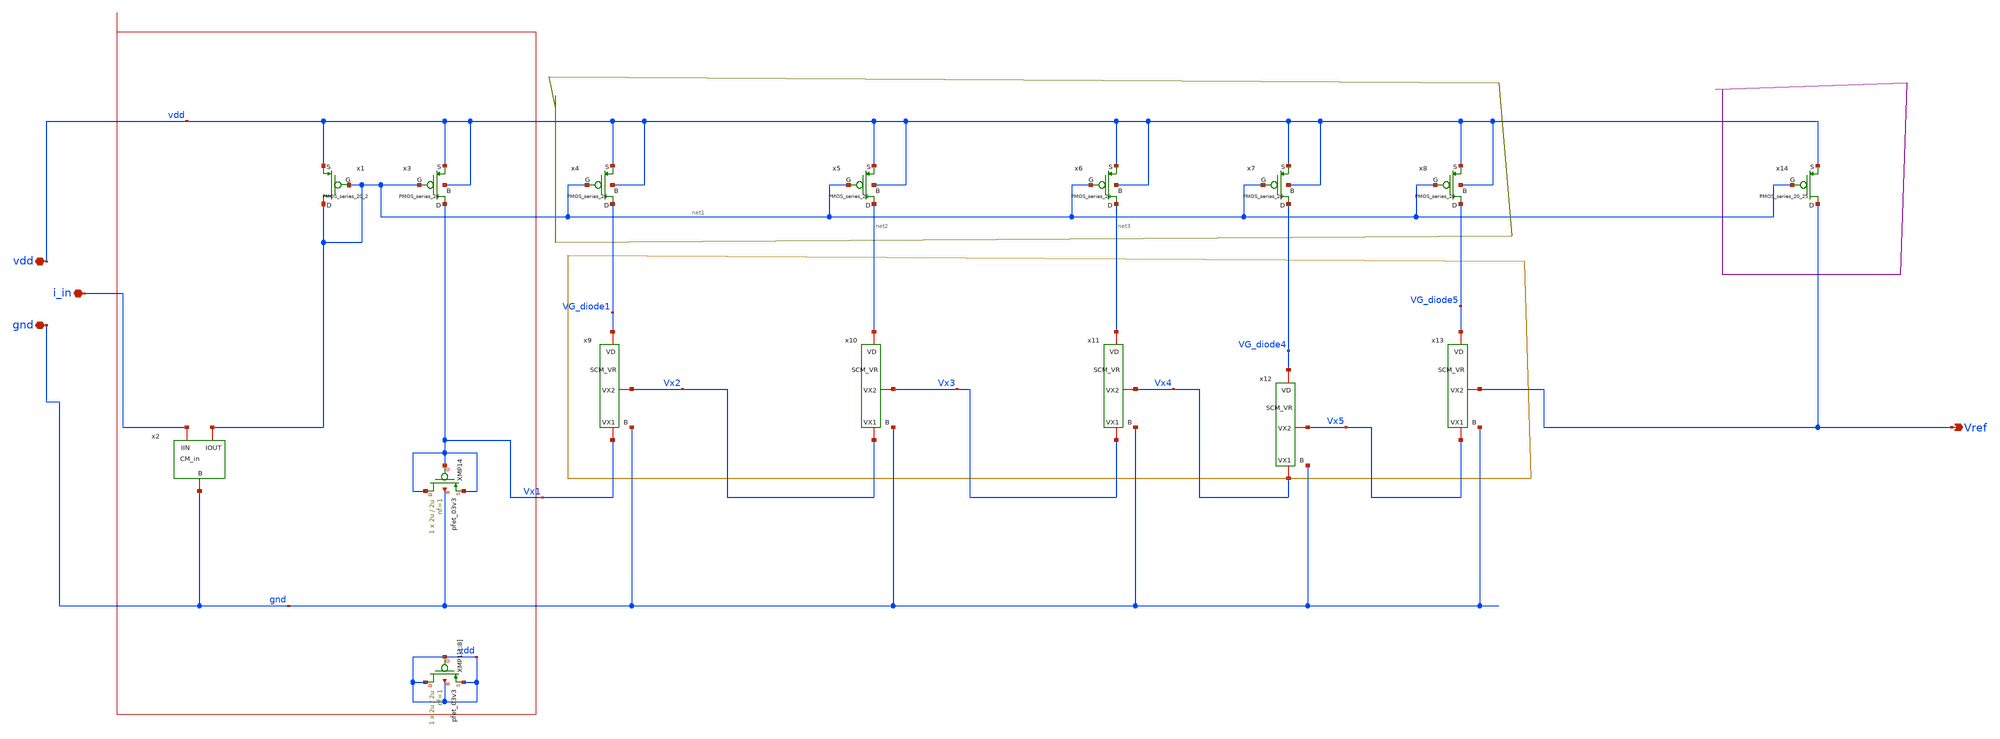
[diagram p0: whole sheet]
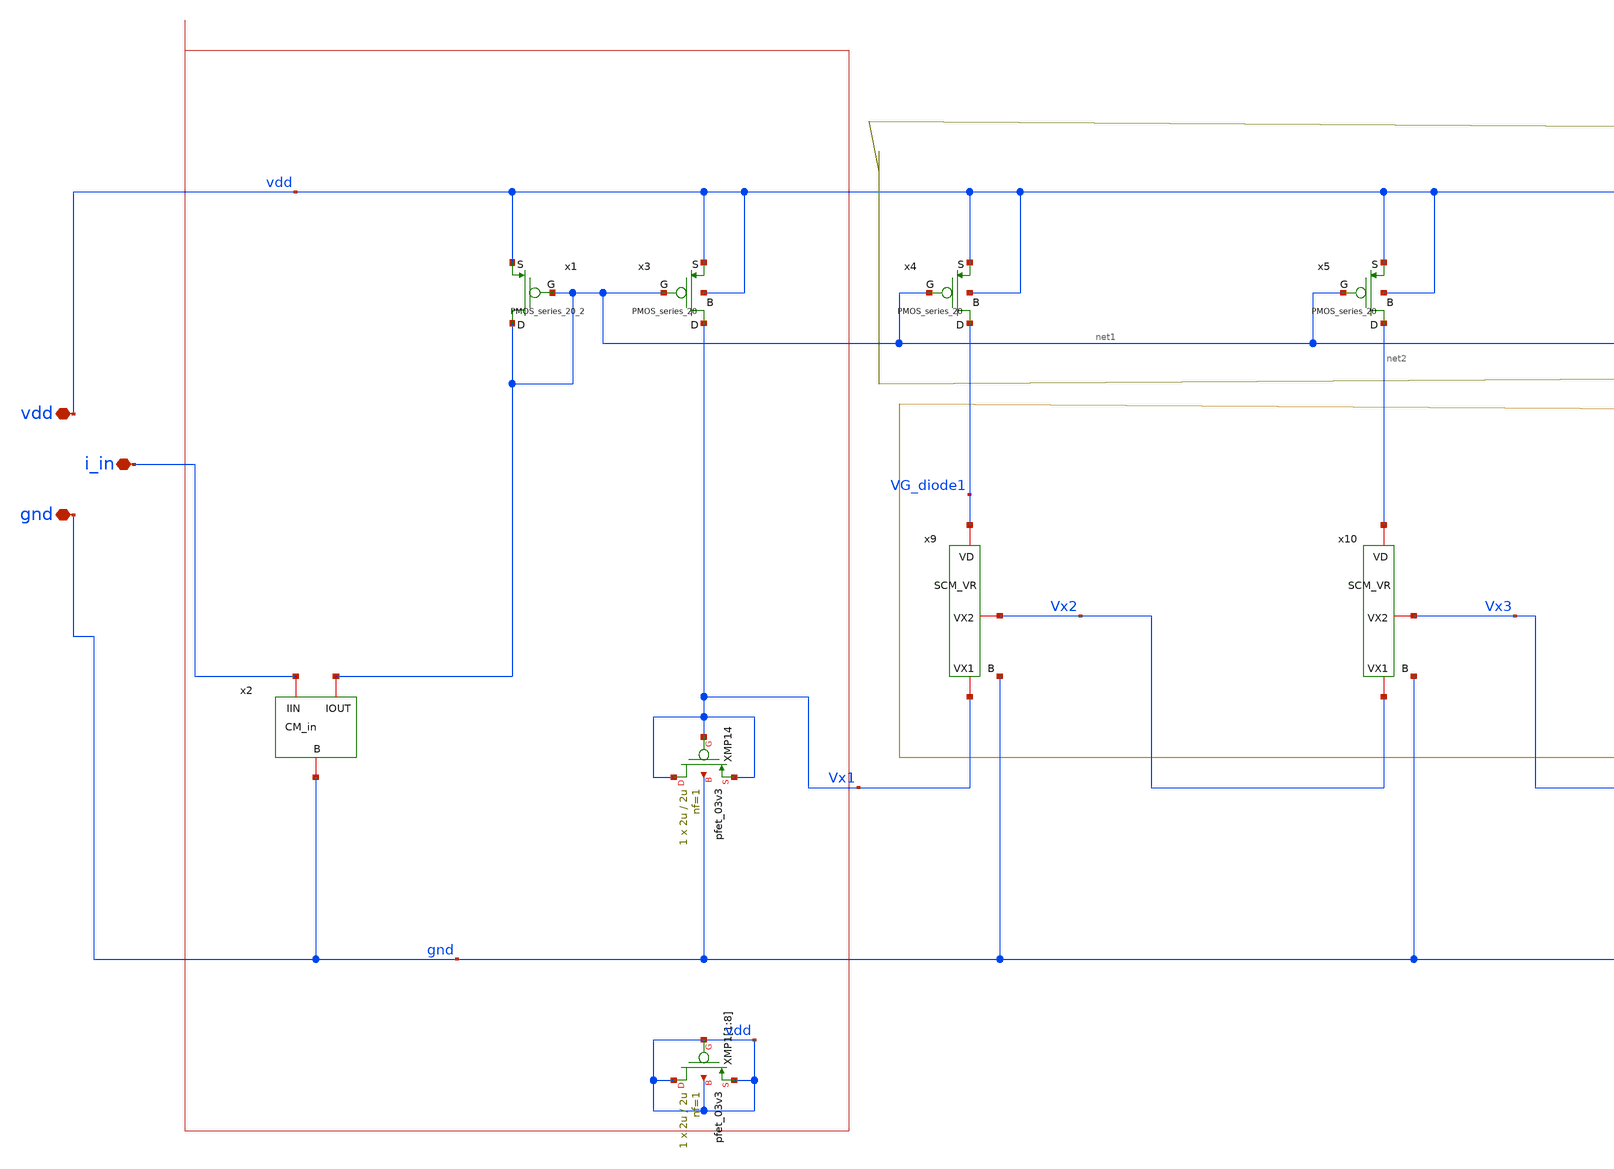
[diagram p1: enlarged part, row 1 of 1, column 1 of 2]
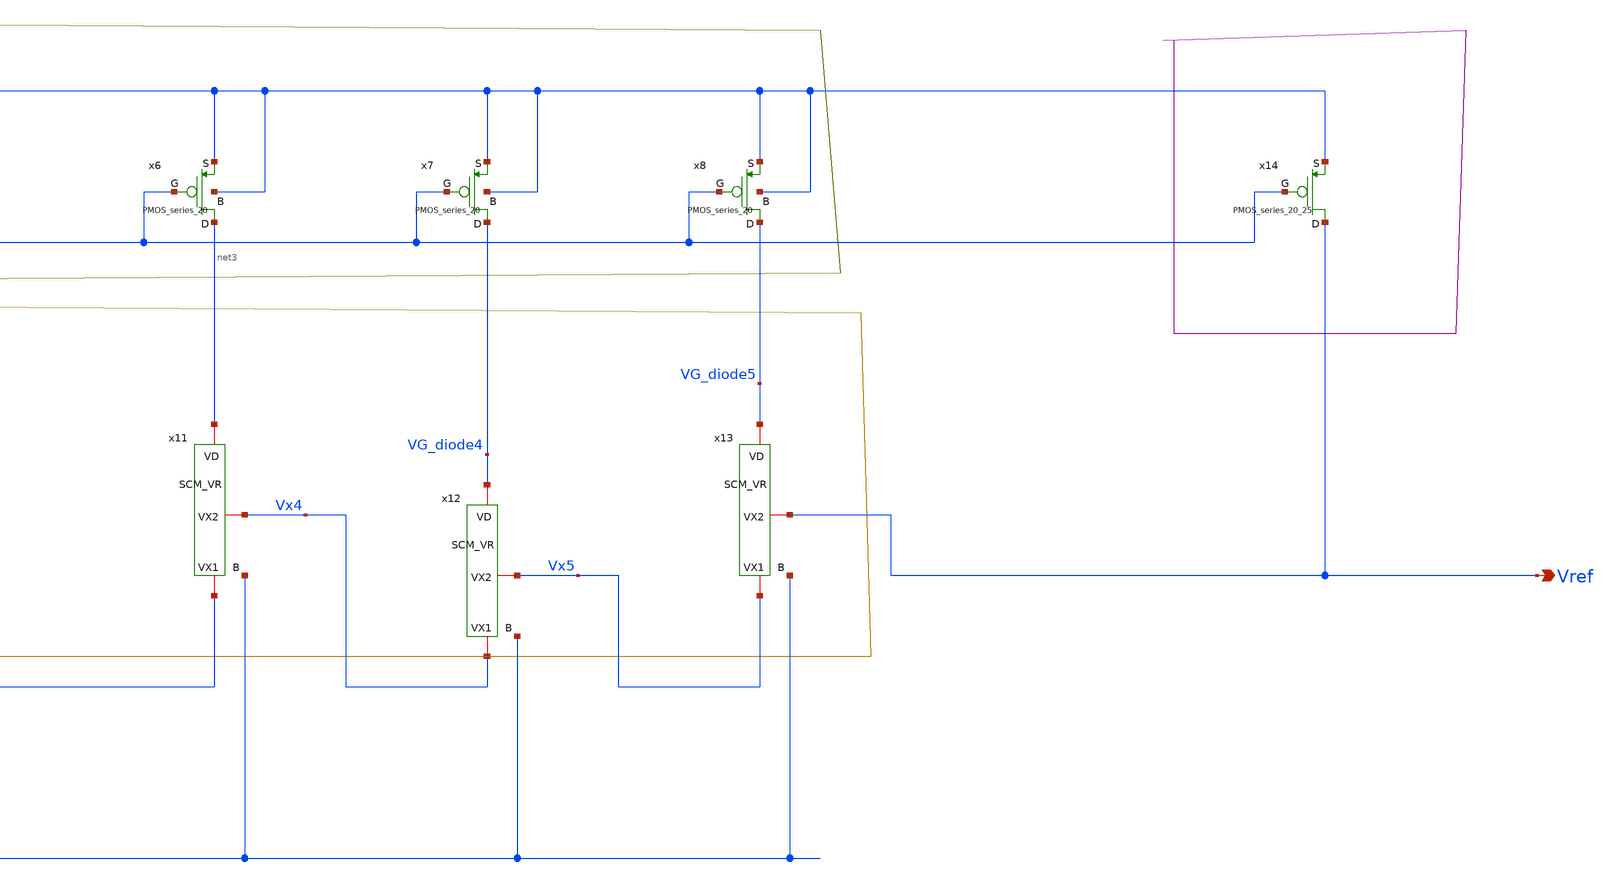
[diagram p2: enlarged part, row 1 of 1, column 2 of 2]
** sch_path: Voltage_Reference/symbols_vr/Voltage_Reference.sch
**.subckt Voltage_Reference i_in vdd gnd Vref
*.iopin i_in
*.iopin vdd
*.iopin gnd
*.opin Vref
XMP14 Vx1 Vx1 Vx1 gnd pfet_03v3 L=2u W=2u nf=1 ad='int((nf+1)/2) * W/nf * 0.18u' as='int((nf+2)/2) * W/nf * 0.18u'
+ pd='2*int((nf+1)/2) * (W/nf + 0.18u)' ps='2*int((nf+2)/2) * (W/nf + 0.18u)' nrd='0.18u / W' nrs='0.18u / W'
+ sa=0 sb=0 sd=0 m=1
x3 vdd Vx1 vdd net1 PMOS_series_20
x4 vdd VG_diode1 vdd net1 PMOS_series_20
x5 vdd net2 vdd net1 PMOS_series_20
x6 vdd net3 vdd net1 PMOS_series_20
x7 vdd VG_diode4 vdd net1 PMOS_series_20
x8 vdd VG_diode5 vdd net1 PMOS_series_20
x9 VG_diode1 Vx1 Vx2 gnd SCM_VR
x10 net2 Vx2 Vx3 gnd SCM_VR
x11 net3 Vx3 Vx4 gnd SCM_VR
x12 VG_diode4 Vx4 Vx5 gnd SCM_VR
x13 VG_diode5 Vx5 Vref gnd SCM_VR
x14 vdd Vref net1 PMOS_series_20_25
x1 vdd net1 net1 PMOS_series_20_2
x2 i_in net1 gnd CM_in
XMP1[1] vdd vdd vdd vdd pfet_03v3 L=2u W=2u nf=1 ad='int((nf+1)/2) * W/nf * 0.18u' as='int((nf+2)/2) * W/nf * 0.18u'
+ pd='2*int((nf+1)/2) * (W/nf + 0.18u)' ps='2*int((nf+2)/2) * (W/nf + 0.18u)' nrd='0.18u / W' nrs='0.18u / W'
+ sa=0 sb=0 sd=0 m=1
XMP1[2] vdd vdd vdd vdd pfet_03v3 L=2u W=2u nf=1 ad='int((nf+1)/2) * W/nf * 0.18u' as='int((nf+2)/2) * W/nf * 0.18u'
+ pd='2*int((nf+1)/2) * (W/nf + 0.18u)' ps='2*int((nf+2)/2) * (W/nf + 0.18u)' nrd='0.18u / W' nrs='0.18u / W'
+ sa=0 sb=0 sd=0 m=1
XMP1[3] vdd vdd vdd vdd pfet_03v3 L=2u W=2u nf=1 ad='int((nf+1)/2) * W/nf * 0.18u' as='int((nf+2)/2) * W/nf * 0.18u'
+ pd='2*int((nf+1)/2) * (W/nf + 0.18u)' ps='2*int((nf+2)/2) * (W/nf + 0.18u)' nrd='0.18u / W' nrs='0.18u / W'
+ sa=0 sb=0 sd=0 m=1
XMP1[4] vdd vdd vdd vdd pfet_03v3 L=2u W=2u nf=1 ad='int((nf+1)/2) * W/nf * 0.18u' as='int((nf+2)/2) * W/nf * 0.18u'
+ pd='2*int((nf+1)/2) * (W/nf + 0.18u)' ps='2*int((nf+2)/2) * (W/nf + 0.18u)' nrd='0.18u / W' nrs='0.18u / W'
+ sa=0 sb=0 sd=0 m=1
XMP1[5] vdd vdd vdd vdd pfet_03v3 L=2u W=2u nf=1 ad='int((nf+1)/2) * W/nf * 0.18u' as='int((nf+2)/2) * W/nf * 0.18u'
+ pd='2*int((nf+1)/2) * (W/nf + 0.18u)' ps='2*int((nf+2)/2) * (W/nf + 0.18u)' nrd='0.18u / W' nrs='0.18u / W'
+ sa=0 sb=0 sd=0 m=1
XMP1[6] vdd vdd vdd vdd pfet_03v3 L=2u W=2u nf=1 ad='int((nf+1)/2) * W/nf * 0.18u' as='int((nf+2)/2) * W/nf * 0.18u'
+ pd='2*int((nf+1)/2) * (W/nf + 0.18u)' ps='2*int((nf+2)/2) * (W/nf + 0.18u)' nrd='0.18u / W' nrs='0.18u / W'
+ sa=0 sb=0 sd=0 m=1
XMP1[7] vdd vdd vdd vdd pfet_03v3 L=2u W=2u nf=1 ad='int((nf+1)/2) * W/nf * 0.18u' as='int((nf+2)/2) * W/nf * 0.18u'
+ pd='2*int((nf+1)/2) * (W/nf + 0.18u)' ps='2*int((nf+2)/2) * (W/nf + 0.18u)' nrd='0.18u / W' nrs='0.18u / W'
+ sa=0 sb=0 sd=0 m=1
XMP1[8] vdd vdd vdd vdd pfet_03v3 L=2u W=2u nf=1 ad='int((nf+1)/2) * W/nf * 0.18u' as='int((nf+2)/2) * W/nf * 0.18u'
+ pd='2*int((nf+1)/2) * (W/nf + 0.18u)' ps='2*int((nf+2)/2) * (W/nf + 0.18u)' nrd='0.18u / W' nrs='0.18u / W'
+ sa=0 sb=0 sd=0 m=1
**.ends

* expanding   symbol:  symbols_vr/PMOS_series_20.sym # of pins=4
** sym_path: Voltage_Reference/symbols_vr/PMOS_series_20.sym
** sch_path: Voltage_Reference/symbols_vr/PMOS_series_20.sch
.subckt PMOS_series_20 S D B G
*.iopin S
*.iopin D
*.iopin B
*.iopin G
XMP1 net1 G S B pfet_03v3 L=2u W=2u nf=1 ad='int((nf+1)/2) * W/nf * 0.18u' as='int((nf+2)/2) * W/nf * 0.18u'
+ pd='2*int((nf+1)/2) * (W/nf + 0.18u)' ps='2*int((nf+2)/2) * (W/nf + 0.18u)' nrd='0.18u / W' nrs='0.18u / W'
+ sa=0 sb=0 sd=0 m=1
XMP2 net3 G net1 B pfet_03v3 L=2u W=2u nf=1 ad='int((nf+1)/2) * W/nf * 0.18u' as='int((nf+2)/2) * W/nf * 0.18u'
+ pd='2*int((nf+1)/2) * (W/nf + 0.18u)' ps='2*int((nf+2)/2) * (W/nf + 0.18u)' nrd='0.18u / W' nrs='0.18u / W'
+ sa=0 sb=0 sd=0 m=1
XMP3 net2 G net3 B pfet_03v3 L=2u W=2u nf=1 ad='int((nf+1)/2) * W/nf * 0.18u' as='int((nf+2)/2) * W/nf * 0.18u'
+ pd='2*int((nf+1)/2) * (W/nf + 0.18u)' ps='2*int((nf+2)/2) * (W/nf + 0.18u)' nrd='0.18u / W' nrs='0.18u / W'
+ sa=0 sb=0 sd=0 m=1
XMP4 net5 G net2 B pfet_03v3 L=2u W=2u nf=1 ad='int((nf+1)/2) * W/nf * 0.18u' as='int((nf+2)/2) * W/nf * 0.18u'
+ pd='2*int((nf+1)/2) * (W/nf + 0.18u)' ps='2*int((nf+2)/2) * (W/nf + 0.18u)' nrd='0.18u / W' nrs='0.18u / W'
+ sa=0 sb=0 sd=0 m=1
XMP5 net4 G net5 B pfet_03v3 L=2u W=2u nf=1 ad='int((nf+1)/2) * W/nf * 0.18u' as='int((nf+2)/2) * W/nf * 0.18u'
+ pd='2*int((nf+1)/2) * (W/nf + 0.18u)' ps='2*int((nf+2)/2) * (W/nf + 0.18u)' nrd='0.18u / W' nrs='0.18u / W'
+ sa=0 sb=0 sd=0 m=1
XMP6 net7 G net4 B pfet_03v3 L=2u W=2u nf=1 ad='int((nf+1)/2) * W/nf * 0.18u' as='int((nf+2)/2) * W/nf * 0.18u'
+ pd='2*int((nf+1)/2) * (W/nf + 0.18u)' ps='2*int((nf+2)/2) * (W/nf + 0.18u)' nrd='0.18u / W' nrs='0.18u / W'
+ sa=0 sb=0 sd=0 m=1
XMP7 net6 G net7 B pfet_03v3 L=2u W=2u nf=1 ad='int((nf+1)/2) * W/nf * 0.18u' as='int((nf+2)/2) * W/nf * 0.18u'
+ pd='2*int((nf+1)/2) * (W/nf + 0.18u)' ps='2*int((nf+2)/2) * (W/nf + 0.18u)' nrd='0.18u / W' nrs='0.18u / W'
+ sa=0 sb=0 sd=0 m=1
XMP8 net9 G net6 B pfet_03v3 L=2u W=2u nf=1 ad='int((nf+1)/2) * W/nf * 0.18u' as='int((nf+2)/2) * W/nf * 0.18u'
+ pd='2*int((nf+1)/2) * (W/nf + 0.18u)' ps='2*int((nf+2)/2) * (W/nf + 0.18u)' nrd='0.18u / W' nrs='0.18u / W'
+ sa=0 sb=0 sd=0 m=1
XMP9 net8 G net9 B pfet_03v3 L=2u W=2u nf=1 ad='int((nf+1)/2) * W/nf * 0.18u' as='int((nf+2)/2) * W/nf * 0.18u'
+ pd='2*int((nf+1)/2) * (W/nf + 0.18u)' ps='2*int((nf+2)/2) * (W/nf + 0.18u)' nrd='0.18u / W' nrs='0.18u / W'
+ sa=0 sb=0 sd=0 m=1
XMP10 net19 G net8 B pfet_03v3 L=2u W=2u nf=1 ad='int((nf+1)/2) * W/nf * 0.18u' as='int((nf+2)/2) * W/nf * 0.18u'
+ pd='2*int((nf+1)/2) * (W/nf + 0.18u)' ps='2*int((nf+2)/2) * (W/nf + 0.18u)' nrd='0.18u / W' nrs='0.18u / W'
+ sa=0 sb=0 sd=0 m=1
XMP11 net10 G net19 B pfet_03v3 L=2u W=2u nf=1 ad='int((nf+1)/2) * W/nf * 0.18u' as='int((nf+2)/2) * W/nf * 0.18u'
+ pd='2*int((nf+1)/2) * (W/nf + 0.18u)' ps='2*int((nf+2)/2) * (W/nf + 0.18u)' nrd='0.18u / W' nrs='0.18u / W'
+ sa=0 sb=0 sd=0 m=1
XMP12 net12 G net10 B pfet_03v3 L=2u W=2u nf=1 ad='int((nf+1)/2) * W/nf * 0.18u' as='int((nf+2)/2) * W/nf * 0.18u'
+ pd='2*int((nf+1)/2) * (W/nf + 0.18u)' ps='2*int((nf+2)/2) * (W/nf + 0.18u)' nrd='0.18u / W' nrs='0.18u / W'
+ sa=0 sb=0 sd=0 m=1
XMP13 net11 G net12 B pfet_03v3 L=2u W=2u nf=1 ad='int((nf+1)/2) * W/nf * 0.18u' as='int((nf+2)/2) * W/nf * 0.18u'
+ pd='2*int((nf+1)/2) * (W/nf + 0.18u)' ps='2*int((nf+2)/2) * (W/nf + 0.18u)' nrd='0.18u / W' nrs='0.18u / W'
+ sa=0 sb=0 sd=0 m=1
XMP14 net14 G net11 B pfet_03v3 L=2u W=2u nf=1 ad='int((nf+1)/2) * W/nf * 0.18u' as='int((nf+2)/2) * W/nf * 0.18u'
+ pd='2*int((nf+1)/2) * (W/nf + 0.18u)' ps='2*int((nf+2)/2) * (W/nf + 0.18u)' nrd='0.18u / W' nrs='0.18u / W'
+ sa=0 sb=0 sd=0 m=1
XMP15 net13 G net14 B pfet_03v3 L=2u W=2u nf=1 ad='int((nf+1)/2) * W/nf * 0.18u' as='int((nf+2)/2) * W/nf * 0.18u'
+ pd='2*int((nf+1)/2) * (W/nf + 0.18u)' ps='2*int((nf+2)/2) * (W/nf + 0.18u)' nrd='0.18u / W' nrs='0.18u / W'
+ sa=0 sb=0 sd=0 m=1
XMP16 net16 G net13 B pfet_03v3 L=2u W=2u nf=1 ad='int((nf+1)/2) * W/nf * 0.18u' as='int((nf+2)/2) * W/nf * 0.18u'
+ pd='2*int((nf+1)/2) * (W/nf + 0.18u)' ps='2*int((nf+2)/2) * (W/nf + 0.18u)' nrd='0.18u / W' nrs='0.18u / W'
+ sa=0 sb=0 sd=0 m=1
XMP17 net15 G net16 B pfet_03v3 L=2u W=2u nf=1 ad='int((nf+1)/2) * W/nf * 0.18u' as='int((nf+2)/2) * W/nf * 0.18u'
+ pd='2*int((nf+1)/2) * (W/nf + 0.18u)' ps='2*int((nf+2)/2) * (W/nf + 0.18u)' nrd='0.18u / W' nrs='0.18u / W'
+ sa=0 sb=0 sd=0 m=1
XMP18 net18 G net15 B pfet_03v3 L=2u W=2u nf=1 ad='int((nf+1)/2) * W/nf * 0.18u' as='int((nf+2)/2) * W/nf * 0.18u'
+ pd='2*int((nf+1)/2) * (W/nf + 0.18u)' ps='2*int((nf+2)/2) * (W/nf + 0.18u)' nrd='0.18u / W' nrs='0.18u / W'
+ sa=0 sb=0 sd=0 m=1
XMP19 net17 G net18 B pfet_03v3 L=2u W=2u nf=1 ad='int((nf+1)/2) * W/nf * 0.18u' as='int((nf+2)/2) * W/nf * 0.18u'
+ pd='2*int((nf+1)/2) * (W/nf + 0.18u)' ps='2*int((nf+2)/2) * (W/nf + 0.18u)' nrd='0.18u / W' nrs='0.18u / W'
+ sa=0 sb=0 sd=0 m=1
XMP20 D G net17 B pfet_03v3 L=2u W=2u nf=1 ad='int((nf+1)/2) * W/nf * 0.18u' as='int((nf+2)/2) * W/nf * 0.18u'
+ pd='2*int((nf+1)/2) * (W/nf + 0.18u)' ps='2*int((nf+2)/2) * (W/nf + 0.18u)' nrd='0.18u / W' nrs='0.18u / W'
+ sa=0 sb=0 sd=0 m=1
XMP21[1] B B B B pfet_03v3 L=2u W=2u nf=1 ad='int((nf+1)/2) * W/nf * 0.18u' as='int((nf+2)/2) * W/nf * 0.18u'
+ pd='2*int((nf+1)/2) * (W/nf + 0.18u)' ps='2*int((nf+2)/2) * (W/nf + 0.18u)' nrd='0.18u / W' nrs='0.18u / W'
+ sa=0 sb=0 sd=0 m=1
XMP21[2] B B B B pfet_03v3 L=2u W=2u nf=1 ad='int((nf+1)/2) * W/nf * 0.18u' as='int((nf+2)/2) * W/nf * 0.18u'
+ pd='2*int((nf+1)/2) * (W/nf + 0.18u)' ps='2*int((nf+2)/2) * (W/nf + 0.18u)' nrd='0.18u / W' nrs='0.18u / W'
+ sa=0 sb=0 sd=0 m=1
XMP21[3] B B B B pfet_03v3 L=2u W=2u nf=1 ad='int((nf+1)/2) * W/nf * 0.18u' as='int((nf+2)/2) * W/nf * 0.18u'
+ pd='2*int((nf+1)/2) * (W/nf + 0.18u)' ps='2*int((nf+2)/2) * (W/nf + 0.18u)' nrd='0.18u / W' nrs='0.18u / W'
+ sa=0 sb=0 sd=0 m=1
XMP21[4] B B B B pfet_03v3 L=2u W=2u nf=1 ad='int((nf+1)/2) * W/nf * 0.18u' as='int((nf+2)/2) * W/nf * 0.18u'
+ pd='2*int((nf+1)/2) * (W/nf + 0.18u)' ps='2*int((nf+2)/2) * (W/nf + 0.18u)' nrd='0.18u / W' nrs='0.18u / W'
+ sa=0 sb=0 sd=0 m=1
XMP21[5] B B B B pfet_03v3 L=2u W=2u nf=1 ad='int((nf+1)/2) * W/nf * 0.18u' as='int((nf+2)/2) * W/nf * 0.18u'
+ pd='2*int((nf+1)/2) * (W/nf + 0.18u)' ps='2*int((nf+2)/2) * (W/nf + 0.18u)' nrd='0.18u / W' nrs='0.18u / W'
+ sa=0 sb=0 sd=0 m=1
XMP21[6] B B B B pfet_03v3 L=2u W=2u nf=1 ad='int((nf+1)/2) * W/nf * 0.18u' as='int((nf+2)/2) * W/nf * 0.18u'
+ pd='2*int((nf+1)/2) * (W/nf + 0.18u)' ps='2*int((nf+2)/2) * (W/nf + 0.18u)' nrd='0.18u / W' nrs='0.18u / W'
+ sa=0 sb=0 sd=0 m=1
XMP21[7] B B B B pfet_03v3 L=2u W=2u nf=1 ad='int((nf+1)/2) * W/nf * 0.18u' as='int((nf+2)/2) * W/nf * 0.18u'
+ pd='2*int((nf+1)/2) * (W/nf + 0.18u)' ps='2*int((nf+2)/2) * (W/nf + 0.18u)' nrd='0.18u / W' nrs='0.18u / W'
+ sa=0 sb=0 sd=0 m=1
XMP21[8] B B B B pfet_03v3 L=2u W=2u nf=1 ad='int((nf+1)/2) * W/nf * 0.18u' as='int((nf+2)/2) * W/nf * 0.18u'
+ pd='2*int((nf+1)/2) * (W/nf + 0.18u)' ps='2*int((nf+2)/2) * (W/nf + 0.18u)' nrd='0.18u / W' nrs='0.18u / W'
+ sa=0 sb=0 sd=0 m=1
XMP21[9] B B B B pfet_03v3 L=2u W=2u nf=1 ad='int((nf+1)/2) * W/nf * 0.18u' as='int((nf+2)/2) * W/nf * 0.18u'
+ pd='2*int((nf+1)/2) * (W/nf + 0.18u)' ps='2*int((nf+2)/2) * (W/nf + 0.18u)' nrd='0.18u / W' nrs='0.18u / W'
+ sa=0 sb=0 sd=0 m=1
XMP21[10] B B B B pfet_03v3 L=2u W=2u nf=1 ad='int((nf+1)/2) * W/nf * 0.18u' as='int((nf+2)/2) * W/nf * 0.18u'
+ pd='2*int((nf+1)/2) * (W/nf + 0.18u)' ps='2*int((nf+2)/2) * (W/nf + 0.18u)' nrd='0.18u / W' nrs='0.18u / W'
+ sa=0 sb=0 sd=0 m=1
XMP21[11] B B B B pfet_03v3 L=2u W=2u nf=1 ad='int((nf+1)/2) * W/nf * 0.18u' as='int((nf+2)/2) * W/nf * 0.18u'
+ pd='2*int((nf+1)/2) * (W/nf + 0.18u)' ps='2*int((nf+2)/2) * (W/nf + 0.18u)' nrd='0.18u / W' nrs='0.18u / W'
+ sa=0 sb=0 sd=0 m=1
XMP21[12] B B B B pfet_03v3 L=2u W=2u nf=1 ad='int((nf+1)/2) * W/nf * 0.18u' as='int((nf+2)/2) * W/nf * 0.18u'
+ pd='2*int((nf+1)/2) * (W/nf + 0.18u)' ps='2*int((nf+2)/2) * (W/nf + 0.18u)' nrd='0.18u / W' nrs='0.18u / W'
+ sa=0 sb=0 sd=0 m=1
XMP21[13] B B B B pfet_03v3 L=2u W=2u nf=1 ad='int((nf+1)/2) * W/nf * 0.18u' as='int((nf+2)/2) * W/nf * 0.18u'
+ pd='2*int((nf+1)/2) * (W/nf + 0.18u)' ps='2*int((nf+2)/2) * (W/nf + 0.18u)' nrd='0.18u / W' nrs='0.18u / W'
+ sa=0 sb=0 sd=0 m=1
XMP21[14] B B B B pfet_03v3 L=2u W=2u nf=1 ad='int((nf+1)/2) * W/nf * 0.18u' as='int((nf+2)/2) * W/nf * 0.18u'
+ pd='2*int((nf+1)/2) * (W/nf + 0.18u)' ps='2*int((nf+2)/2) * (W/nf + 0.18u)' nrd='0.18u / W' nrs='0.18u / W'
+ sa=0 sb=0 sd=0 m=1
XMP21[15] B B B B pfet_03v3 L=2u W=2u nf=1 ad='int((nf+1)/2) * W/nf * 0.18u' as='int((nf+2)/2) * W/nf * 0.18u'
+ pd='2*int((nf+1)/2) * (W/nf + 0.18u)' ps='2*int((nf+2)/2) * (W/nf + 0.18u)' nrd='0.18u / W' nrs='0.18u / W'
+ sa=0 sb=0 sd=0 m=1
XMP21[16] B B B B pfet_03v3 L=2u W=2u nf=1 ad='int((nf+1)/2) * W/nf * 0.18u' as='int((nf+2)/2) * W/nf * 0.18u'
+ pd='2*int((nf+1)/2) * (W/nf + 0.18u)' ps='2*int((nf+2)/2) * (W/nf + 0.18u)' nrd='0.18u / W' nrs='0.18u / W'
+ sa=0 sb=0 sd=0 m=1
XMP21[17] B B B B pfet_03v3 L=2u W=2u nf=1 ad='int((nf+1)/2) * W/nf * 0.18u' as='int((nf+2)/2) * W/nf * 0.18u'
+ pd='2*int((nf+1)/2) * (W/nf + 0.18u)' ps='2*int((nf+2)/2) * (W/nf + 0.18u)' nrd='0.18u / W' nrs='0.18u / W'
+ sa=0 sb=0 sd=0 m=1
XMP21[18] B B B B pfet_03v3 L=2u W=2u nf=1 ad='int((nf+1)/2) * W/nf * 0.18u' as='int((nf+2)/2) * W/nf * 0.18u'
+ pd='2*int((nf+1)/2) * (W/nf + 0.18u)' ps='2*int((nf+2)/2) * (W/nf + 0.18u)' nrd='0.18u / W' nrs='0.18u / W'
+ sa=0 sb=0 sd=0 m=1
XMP21[19] B B B B pfet_03v3 L=2u W=2u nf=1 ad='int((nf+1)/2) * W/nf * 0.18u' as='int((nf+2)/2) * W/nf * 0.18u'
+ pd='2*int((nf+1)/2) * (W/nf + 0.18u)' ps='2*int((nf+2)/2) * (W/nf + 0.18u)' nrd='0.18u / W' nrs='0.18u / W'
+ sa=0 sb=0 sd=0 m=1
XMP21[20] B B B B pfet_03v3 L=2u W=2u nf=1 ad='int((nf+1)/2) * W/nf * 0.18u' as='int((nf+2)/2) * W/nf * 0.18u'
+ pd='2*int((nf+1)/2) * (W/nf + 0.18u)' ps='2*int((nf+2)/2) * (W/nf + 0.18u)' nrd='0.18u / W' nrs='0.18u / W'
+ sa=0 sb=0 sd=0 m=1
XMP21[21] B B B B pfet_03v3 L=2u W=2u nf=1 ad='int((nf+1)/2) * W/nf * 0.18u' as='int((nf+2)/2) * W/nf * 0.18u'
+ pd='2*int((nf+1)/2) * (W/nf + 0.18u)' ps='2*int((nf+2)/2) * (W/nf + 0.18u)' nrd='0.18u / W' nrs='0.18u / W'
+ sa=0 sb=0 sd=0 m=1
XMP21[22] B B B B pfet_03v3 L=2u W=2u nf=1 ad='int((nf+1)/2) * W/nf * 0.18u' as='int((nf+2)/2) * W/nf * 0.18u'
+ pd='2*int((nf+1)/2) * (W/nf + 0.18u)' ps='2*int((nf+2)/2) * (W/nf + 0.18u)' nrd='0.18u / W' nrs='0.18u / W'
+ sa=0 sb=0 sd=0 m=1
.ends


* expanding   symbol:  symbols_vr/SCM_VR.sym # of pins=4
** sym_path: Voltage_Reference/symbols_vr/SCM_VR.sym
** sch_path: Voltage_Reference/symbols_vr/SCM_VR.sch
.subckt SCM_VR VD VX1 VX2 B
*.iopin VD
*.iopin VX1
*.iopin VX2
*.iopin B
XMN1[1] VD VD VX2 B nfet_03v3 L=2u W=2u nf=1 ad='int((nf+1)/2) * W/nf * 0.18u' as='int((nf+2)/2) * W/nf * 0.18u'
+ pd='2*int((nf+1)/2) * (W/nf + 0.18u)' ps='2*int((nf+2)/2) * (W/nf + 0.18u)' nrd='0.18u / W' nrs='0.18u / W'
+ sa=0 sb=0 sd=0 m=1
XMN1[2] VD VD VX2 B nfet_03v3 L=2u W=2u nf=1 ad='int((nf+1)/2) * W/nf * 0.18u' as='int((nf+2)/2) * W/nf * 0.18u'
+ pd='2*int((nf+1)/2) * (W/nf + 0.18u)' ps='2*int((nf+2)/2) * (W/nf + 0.18u)' nrd='0.18u / W' nrs='0.18u / W'
+ sa=0 sb=0 sd=0 m=1
XMN1[3] VD VD VX2 B nfet_03v3 L=2u W=2u nf=1 ad='int((nf+1)/2) * W/nf * 0.18u' as='int((nf+2)/2) * W/nf * 0.18u'
+ pd='2*int((nf+1)/2) * (W/nf + 0.18u)' ps='2*int((nf+2)/2) * (W/nf + 0.18u)' nrd='0.18u / W' nrs='0.18u / W'
+ sa=0 sb=0 sd=0 m=1
XMN1[4] VD VD VX2 B nfet_03v3 L=2u W=2u nf=1 ad='int((nf+1)/2) * W/nf * 0.18u' as='int((nf+2)/2) * W/nf * 0.18u'
+ pd='2*int((nf+1)/2) * (W/nf + 0.18u)' ps='2*int((nf+2)/2) * (W/nf + 0.18u)' nrd='0.18u / W' nrs='0.18u / W'
+ sa=0 sb=0 sd=0 m=1
XMN1[5] VD VD VX2 B nfet_03v3 L=2u W=2u nf=1 ad='int((nf+1)/2) * W/nf * 0.18u' as='int((nf+2)/2) * W/nf * 0.18u'
+ pd='2*int((nf+1)/2) * (W/nf + 0.18u)' ps='2*int((nf+2)/2) * (W/nf + 0.18u)' nrd='0.18u / W' nrs='0.18u / W'
+ sa=0 sb=0 sd=0 m=1
XMN2 VX2 VD VX1 B nfet_03v3 L=2u W=2u nf=1 ad='int((nf+1)/2) * W/nf * 0.18u' as='int((nf+2)/2) * W/nf * 0.18u'
+ pd='2*int((nf+1)/2) * (W/nf + 0.18u)' ps='2*int((nf+2)/2) * (W/nf + 0.18u)' nrd='0.18u / W' nrs='0.18u / W'
+ sa=0 sb=0 sd=0 m=1
XMN2[1] B B B B nfet_03v3 L=2u W=2u nf=1 ad='int((nf+1)/2) * W/nf * 0.18u' as='int((nf+2)/2) * W/nf * 0.18u'
+ pd='2*int((nf+1)/2) * (W/nf + 0.18u)' ps='2*int((nf+2)/2) * (W/nf + 0.18u)' nrd='0.18u / W' nrs='0.18u / W'
+ sa=0 sb=0 sd=0 m=1
XMN2[2] B B B B nfet_03v3 L=2u W=2u nf=1 ad='int((nf+1)/2) * W/nf * 0.18u' as='int((nf+2)/2) * W/nf * 0.18u'
+ pd='2*int((nf+1)/2) * (W/nf + 0.18u)' ps='2*int((nf+2)/2) * (W/nf + 0.18u)' nrd='0.18u / W' nrs='0.18u / W'
+ sa=0 sb=0 sd=0 m=1
XMN2[3] B B B B nfet_03v3 L=2u W=2u nf=1 ad='int((nf+1)/2) * W/nf * 0.18u' as='int((nf+2)/2) * W/nf * 0.18u'
+ pd='2*int((nf+1)/2) * (W/nf + 0.18u)' ps='2*int((nf+2)/2) * (W/nf + 0.18u)' nrd='0.18u / W' nrs='0.18u / W'
+ sa=0 sb=0 sd=0 m=1
XMN2[4] B B B B nfet_03v3 L=2u W=2u nf=1 ad='int((nf+1)/2) * W/nf * 0.18u' as='int((nf+2)/2) * W/nf * 0.18u'
+ pd='2*int((nf+1)/2) * (W/nf + 0.18u)' ps='2*int((nf+2)/2) * (W/nf + 0.18u)' nrd='0.18u / W' nrs='0.18u / W'
+ sa=0 sb=0 sd=0 m=1
XMN2[5] B B B B nfet_03v3 L=2u W=2u nf=1 ad='int((nf+1)/2) * W/nf * 0.18u' as='int((nf+2)/2) * W/nf * 0.18u'
+ pd='2*int((nf+1)/2) * (W/nf + 0.18u)' ps='2*int((nf+2)/2) * (W/nf + 0.18u)' nrd='0.18u / W' nrs='0.18u / W'
+ sa=0 sb=0 sd=0 m=1
XMN2[6] B B B B nfet_03v3 L=2u W=2u nf=1 ad='int((nf+1)/2) * W/nf * 0.18u' as='int((nf+2)/2) * W/nf * 0.18u'
+ pd='2*int((nf+1)/2) * (W/nf + 0.18u)' ps='2*int((nf+2)/2) * (W/nf + 0.18u)' nrd='0.18u / W' nrs='0.18u / W'
+ sa=0 sb=0 sd=0 m=1
XMN2[7] B B B B nfet_03v3 L=2u W=2u nf=1 ad='int((nf+1)/2) * W/nf * 0.18u' as='int((nf+2)/2) * W/nf * 0.18u'
+ pd='2*int((nf+1)/2) * (W/nf + 0.18u)' ps='2*int((nf+2)/2) * (W/nf + 0.18u)' nrd='0.18u / W' nrs='0.18u / W'
+ sa=0 sb=0 sd=0 m=1
XMN2[8] B B B B nfet_03v3 L=2u W=2u nf=1 ad='int((nf+1)/2) * W/nf * 0.18u' as='int((nf+2)/2) * W/nf * 0.18u'
+ pd='2*int((nf+1)/2) * (W/nf + 0.18u)' ps='2*int((nf+2)/2) * (W/nf + 0.18u)' nrd='0.18u / W' nrs='0.18u / W'
+ sa=0 sb=0 sd=0 m=1
XMN2[9] B B B B nfet_03v3 L=2u W=2u nf=1 ad='int((nf+1)/2) * W/nf * 0.18u' as='int((nf+2)/2) * W/nf * 0.18u'
+ pd='2*int((nf+1)/2) * (W/nf + 0.18u)' ps='2*int((nf+2)/2) * (W/nf + 0.18u)' nrd='0.18u / W' nrs='0.18u / W'
+ sa=0 sb=0 sd=0 m=1
XMN2[10] B B B B nfet_03v3 L=2u W=2u nf=1 ad='int((nf+1)/2) * W/nf * 0.18u' as='int((nf+2)/2) * W/nf * 0.18u'
+ pd='2*int((nf+1)/2) * (W/nf + 0.18u)' ps='2*int((nf+2)/2) * (W/nf + 0.18u)' nrd='0.18u / W' nrs='0.18u / W'
+ sa=0 sb=0 sd=0 m=1
XMN2[11] B B B B nfet_03v3 L=2u W=2u nf=1 ad='int((nf+1)/2) * W/nf * 0.18u' as='int((nf+2)/2) * W/nf * 0.18u'
+ pd='2*int((nf+1)/2) * (W/nf + 0.18u)' ps='2*int((nf+2)/2) * (W/nf + 0.18u)' nrd='0.18u / W' nrs='0.18u / W'
+ sa=0 sb=0 sd=0 m=1
XMN2[12] B B B B nfet_03v3 L=2u W=2u nf=1 ad='int((nf+1)/2) * W/nf * 0.18u' as='int((nf+2)/2) * W/nf * 0.18u'
+ pd='2*int((nf+1)/2) * (W/nf + 0.18u)' ps='2*int((nf+2)/2) * (W/nf + 0.18u)' nrd='0.18u / W' nrs='0.18u / W'
+ sa=0 sb=0 sd=0 m=1
XMN2[13] B B B B nfet_03v3 L=2u W=2u nf=1 ad='int((nf+1)/2) * W/nf * 0.18u' as='int((nf+2)/2) * W/nf * 0.18u'
+ pd='2*int((nf+1)/2) * (W/nf + 0.18u)' ps='2*int((nf+2)/2) * (W/nf + 0.18u)' nrd='0.18u / W' nrs='0.18u / W'
+ sa=0 sb=0 sd=0 m=1
XMN2[14] B B B B nfet_03v3 L=2u W=2u nf=1 ad='int((nf+1)/2) * W/nf * 0.18u' as='int((nf+2)/2) * W/nf * 0.18u'
+ pd='2*int((nf+1)/2) * (W/nf + 0.18u)' ps='2*int((nf+2)/2) * (W/nf + 0.18u)' nrd='0.18u / W' nrs='0.18u / W'
+ sa=0 sb=0 sd=0 m=1
XMN2[15] B B B B nfet_03v3 L=2u W=2u nf=1 ad='int((nf+1)/2) * W/nf * 0.18u' as='int((nf+2)/2) * W/nf * 0.18u'
+ pd='2*int((nf+1)/2) * (W/nf + 0.18u)' ps='2*int((nf+2)/2) * (W/nf + 0.18u)' nrd='0.18u / W' nrs='0.18u / W'
+ sa=0 sb=0 sd=0 m=1
XMN2[16] B B B B nfet_03v3 L=2u W=2u nf=1 ad='int((nf+1)/2) * W/nf * 0.18u' as='int((nf+2)/2) * W/nf * 0.18u'
+ pd='2*int((nf+1)/2) * (W/nf + 0.18u)' ps='2*int((nf+2)/2) * (W/nf + 0.18u)' nrd='0.18u / W' nrs='0.18u / W'
+ sa=0 sb=0 sd=0 m=1
XMN2[17] B B B B nfet_03v3 L=2u W=2u nf=1 ad='int((nf+1)/2) * W/nf * 0.18u' as='int((nf+2)/2) * W/nf * 0.18u'
+ pd='2*int((nf+1)/2) * (W/nf + 0.18u)' ps='2*int((nf+2)/2) * (W/nf + 0.18u)' nrd='0.18u / W' nrs='0.18u / W'
+ sa=0 sb=0 sd=0 m=1
XMN2[18] B B B B nfet_03v3 L=2u W=2u nf=1 ad='int((nf+1)/2) * W/nf * 0.18u' as='int((nf+2)/2) * W/nf * 0.18u'
+ pd='2*int((nf+1)/2) * (W/nf + 0.18u)' ps='2*int((nf+2)/2) * (W/nf + 0.18u)' nrd='0.18u / W' nrs='0.18u / W'
+ sa=0 sb=0 sd=0 m=1
.ends


* expanding   symbol:  symbols_vr/PMOS_series_20_25.sym # of pins=3
** sym_path: Voltage_Reference/symbols_vr/PMOS_series_20_25.sym
** sch_path: Voltage_Reference/symbols_vr/PMOS_series_20_25.sch
.subckt PMOS_series_20_25 S D G
*.iopin S
*.iopin D
*.iopin G
x1[1] S D S G PMOS_series_20
x1[2] S D S G PMOS_series_20
x1[3] S D S G PMOS_series_20
x1[4] S D S G PMOS_series_20
x1[5] S D S G PMOS_series_20
x1[6] S D S G PMOS_series_20
x1[7] S D S G PMOS_series_20
x1[8] S D S G PMOS_series_20
x1[9] S D S G PMOS_series_20
x1[10] S D S G PMOS_series_20
x1[11] S D S G PMOS_series_20
x1[12] S D S G PMOS_series_20
x1[13] S D S G PMOS_series_20
x1[14] S D S G PMOS_series_20
x1[15] S D S G PMOS_series_20
x1[16] S D S G PMOS_series_20
x1[17] S D S G PMOS_series_20
x1[18] S D S G PMOS_series_20
x1[19] S D S G PMOS_series_20
x1[20] S D S G PMOS_series_20
x1[21] S D S G PMOS_series_20
x1[22] S D S G PMOS_series_20
x1[23] S D S G PMOS_series_20
x1[24] S D S G PMOS_series_20
x1[25] S D S G PMOS_series_20
.ends


* expanding   symbol:  symbols_vr/PMOS_series_20_2.sym # of pins=3
** sym_path: Voltage_Reference/symbols_vr/PMOS_series_20_2.sym
** sch_path: Voltage_Reference/symbols_vr/PMOS_series_20_2.sch
.subckt PMOS_series_20_2 S D G
*.iopin S
*.iopin D
*.iopin G
x1 S net1 S G PMOS_series_20
x2 net1 D S G PMOS_series_20
.ends


* expanding   symbol:  symbols_vr/CM_in.sym # of pins=3
** sym_path: Voltage_Reference/symbols_vr/CM_in.sym
** sch_path: Voltage_Reference/symbols_vr/CM_in.sch
.subckt CM_in IIN IOUT B
*.iopin IIN
*.iopin IOUT
*.iopin B
XMN7 IOUT IIN net1 B nfet_03v3 L=2u W=2u nf=1 ad='int((nf+1)/2) * W/nf * 0.18u' as='int((nf+2)/2) * W/nf * 0.18u'
+ pd='2*int((nf+1)/2) * (W/nf + 0.18u)' ps='2*int((nf+2)/2) * (W/nf + 0.18u)' nrd='0.18u / W' nrs='0.18u / W'
+ sa=0 sb=0 sd=0 m=1
XMN8 net1 net2 B B nfet_03v3 L=2u W=2u nf=1 ad='int((nf+1)/2) * W/nf * 0.18u' as='int((nf+2)/2) * W/nf * 0.18u'
+ pd='2*int((nf+1)/2) * (W/nf + 0.18u)' ps='2*int((nf+2)/2) * (W/nf + 0.18u)' nrd='0.18u / W' nrs='0.18u / W'
+ sa=0 sb=0 sd=0 m=1
XMN11 IIN IIN net2 B nfet_03v3 L=2u W=2u nf=1 ad='int((nf+1)/2) * W/nf * 0.18u' as='int((nf+2)/2) * W/nf * 0.18u'
+ pd='2*int((nf+1)/2) * (W/nf + 0.18u)' ps='2*int((nf+2)/2) * (W/nf + 0.18u)' nrd='0.18u / W' nrs='0.18u / W'
+ sa=0 sb=0 sd=0 m=1
XMN12 net2 net2 B B nfet_03v3 L=2u W=2u nf=1 ad='int((nf+1)/2) * W/nf * 0.18u' as='int((nf+2)/2) * W/nf * 0.18u'
+ pd='2*int((nf+1)/2) * (W/nf + 0.18u)' ps='2*int((nf+2)/2) * (W/nf + 0.18u)' nrd='0.18u / W' nrs='0.18u / W'
+ sa=0 sb=0 sd=0 m=1
XMN1[1] B B B B nfet_03v3 L=2u W=2u nf=1 ad='int((nf+1)/2) * W/nf * 0.18u' as='int((nf+2)/2) * W/nf * 0.18u'
+ pd='2*int((nf+1)/2) * (W/nf + 0.18u)' ps='2*int((nf+2)/2) * (W/nf + 0.18u)' nrd='0.18u / W' nrs='0.18u / W'
+ sa=0 sb=0 sd=0 m=1
XMN1[2] B B B B nfet_03v3 L=2u W=2u nf=1 ad='int((nf+1)/2) * W/nf * 0.18u' as='int((nf+2)/2) * W/nf * 0.18u'
+ pd='2*int((nf+1)/2) * (W/nf + 0.18u)' ps='2*int((nf+2)/2) * (W/nf + 0.18u)' nrd='0.18u / W' nrs='0.18u / W'
+ sa=0 sb=0 sd=0 m=1
XMN1[3] B B B B nfet_03v3 L=2u W=2u nf=1 ad='int((nf+1)/2) * W/nf * 0.18u' as='int((nf+2)/2) * W/nf * 0.18u'
+ pd='2*int((nf+1)/2) * (W/nf + 0.18u)' ps='2*int((nf+2)/2) * (W/nf + 0.18u)' nrd='0.18u / W' nrs='0.18u / W'
+ sa=0 sb=0 sd=0 m=1
XMN1[4] B B B B nfet_03v3 L=2u W=2u nf=1 ad='int((nf+1)/2) * W/nf * 0.18u' as='int((nf+2)/2) * W/nf * 0.18u'
+ pd='2*int((nf+1)/2) * (W/nf + 0.18u)' ps='2*int((nf+2)/2) * (W/nf + 0.18u)' nrd='0.18u / W' nrs='0.18u / W'
+ sa=0 sb=0 sd=0 m=1
XMN1[5] B B B B nfet_03v3 L=2u W=2u nf=1 ad='int((nf+1)/2) * W/nf * 0.18u' as='int((nf+2)/2) * W/nf * 0.18u'
+ pd='2*int((nf+1)/2) * (W/nf + 0.18u)' ps='2*int((nf+2)/2) * (W/nf + 0.18u)' nrd='0.18u / W' nrs='0.18u / W'
+ sa=0 sb=0 sd=0 m=1
XMN1[6] B B B B nfet_03v3 L=2u W=2u nf=1 ad='int((nf+1)/2) * W/nf * 0.18u' as='int((nf+2)/2) * W/nf * 0.18u'
+ pd='2*int((nf+1)/2) * (W/nf + 0.18u)' ps='2*int((nf+2)/2) * (W/nf + 0.18u)' nrd='0.18u / W' nrs='0.18u / W'
+ sa=0 sb=0 sd=0 m=1
XMN1[7] B B B B nfet_03v3 L=2u W=2u nf=1 ad='int((nf+1)/2) * W/nf * 0.18u' as='int((nf+2)/2) * W/nf * 0.18u'
+ pd='2*int((nf+1)/2) * (W/nf + 0.18u)' ps='2*int((nf+2)/2) * (W/nf + 0.18u)' nrd='0.18u / W' nrs='0.18u / W'
+ sa=0 sb=0 sd=0 m=1
XMN1[8] B B B B nfet_03v3 L=2u W=2u nf=1 ad='int((nf+1)/2) * W/nf * 0.18u' as='int((nf+2)/2) * W/nf * 0.18u'
+ pd='2*int((nf+1)/2) * (W/nf + 0.18u)' ps='2*int((nf+2)/2) * (W/nf + 0.18u)' nrd='0.18u / W' nrs='0.18u / W'
+ sa=0 sb=0 sd=0 m=1
XMN1[9] B B B B nfet_03v3 L=2u W=2u nf=1 ad='int((nf+1)/2) * W/nf * 0.18u' as='int((nf+2)/2) * W/nf * 0.18u'
+ pd='2*int((nf+1)/2) * (W/nf + 0.18u)' ps='2*int((nf+2)/2) * (W/nf + 0.18u)' nrd='0.18u / W' nrs='0.18u / W'
+ sa=0 sb=0 sd=0 m=1
XMN1[10] B B B B nfet_03v3 L=2u W=2u nf=1 ad='int((nf+1)/2) * W/nf * 0.18u' as='int((nf+2)/2) * W/nf * 0.18u'
+ pd='2*int((nf+1)/2) * (W/nf + 0.18u)' ps='2*int((nf+2)/2) * (W/nf + 0.18u)' nrd='0.18u / W' nrs='0.18u / W'
+ sa=0 sb=0 sd=0 m=1
XMN1[11] B B B B nfet_03v3 L=2u W=2u nf=1 ad='int((nf+1)/2) * W/nf * 0.18u' as='int((nf+2)/2) * W/nf * 0.18u'
+ pd='2*int((nf+1)/2) * (W/nf + 0.18u)' ps='2*int((nf+2)/2) * (W/nf + 0.18u)' nrd='0.18u / W' nrs='0.18u / W'
+ sa=0 sb=0 sd=0 m=1
XMN1[12] B B B B nfet_03v3 L=2u W=2u nf=1 ad='int((nf+1)/2) * W/nf * 0.18u' as='int((nf+2)/2) * W/nf * 0.18u'
+ pd='2*int((nf+1)/2) * (W/nf + 0.18u)' ps='2*int((nf+2)/2) * (W/nf + 0.18u)' nrd='0.18u / W' nrs='0.18u / W'
+ sa=0 sb=0 sd=0 m=1
.ends

.end
